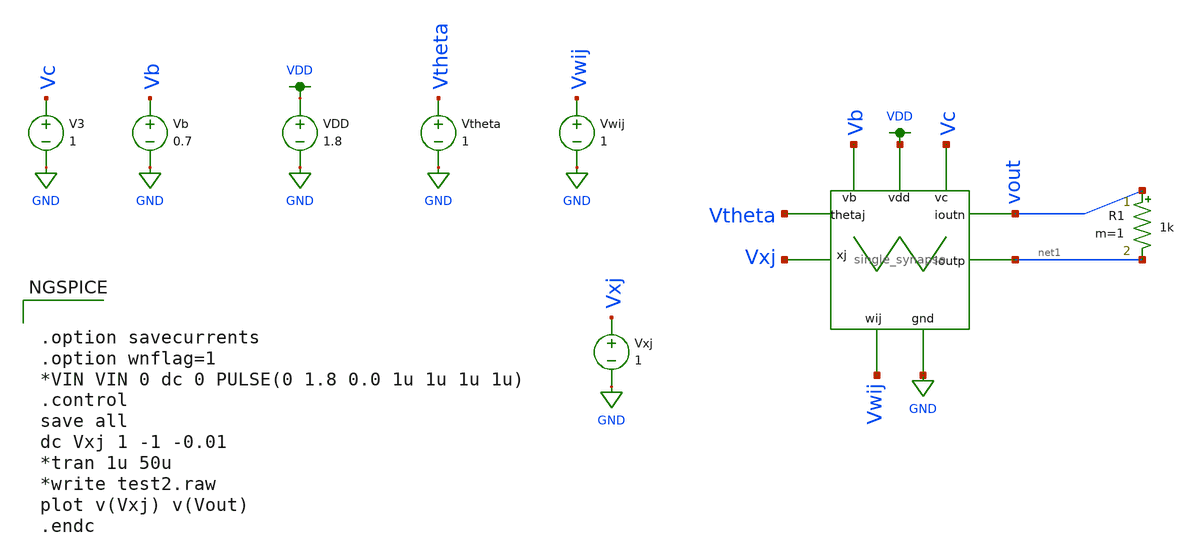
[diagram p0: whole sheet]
** sch_path: test_single_synapse.sch
**.subckt test_single_synapse
VDD VDD GND 1.8
Vb Vb GND 0.7
V3 Vc GND 1
W1 Vtheta Vb VDD Vc Vxj GND Vwij vout net1 single_synapse
Vtheta Vtheta GND 1
Vwij Vwij GND 1
Vxj Vxj GND 1
R1 vout net1 1k m=1
**** begin user architecture code


.option savecurrents
.option wnflag=1
*VIN VIN 0 dc 0 PULSE(0 1.8 0.0 1u 1u 1u 1u)
.control
save all
dc Vxj 1 -1 -0.01
*tran 1u 50u
*write test2.raw
plot v(Vxj) v(Vout)
.endc



.option wnflag=1
.lib ~/skywater/skywater-pdk/libraries/sky130_fd_pr_ngspice/latest/models/sky130.lib.spice tt

**** end user architecture code
**.ends

* expanding   symbol:  /home/ttuser/image_processing_final/single_synapse.sym # of pins=9
** sym_path: single_synapse.sym
** sch_path: single_synapse.sch
.subckt single_synapse thetaj Vb Vdd Vc xj GND Wij Ioutn Ioutp
*.iopin Ioutn
*.iopin Ioutp
*.iopin thetaj
*.iopin xj
*.iopin Wij
*.iopin Vb
*.iopin Vc
*.iopin GND
*.iopin Vdd
XM1 Ioutn Ioutn Vdd VDD sky130_fd_pr__pfet_01v8 L=0.15 W=1 nf=1 ad='int((nf+1)/2) * W/nf * 0.29' as='int((nf+2)/2) * W/nf * 0.29'
+ pd='2*int((nf+1)/2) * (W/nf + 0.29)' ps='2*int((nf+2)/2) * (W/nf + 0.29)' nrd='0.29 / W' nrs='0.29 / W'
+ sa=0 sb=0 sd=0 mult=1 m=1
XM2 Ioutp Ioutp Vdd VDD sky130_fd_pr__pfet_01v8 L=0.15 W=1 nf=1 ad='int((nf+1)/2) * W/nf * 0.29' as='int((nf+2)/2) * W/nf * 0.29'
+ pd='2*int((nf+1)/2) * (W/nf + 0.29)' ps='2*int((nf+2)/2) * (W/nf + 0.29)' nrd='0.29 / W' nrs='0.29 / W'
+ sa=0 sb=0 sd=0 mult=1 m=1
XM3 Ioutp xj net1 GND sky130_fd_pr__nfet_01v8 L=0.15 W=1 nf=1 ad='int((nf+1)/2) * W/nf * 0.29' as='int((nf+2)/2) * W/nf * 0.29'
+ pd='2*int((nf+1)/2) * (W/nf + 0.29)' ps='2*int((nf+2)/2) * (W/nf + 0.29)' nrd='0.29 / W' nrs='0.29 / W'
+ sa=0 sb=0 sd=0 mult=1 m=1
XM4 net1 net1 net3 GND sky130_fd_pr__nfet_01v8 L=0.15 W=1 nf=1 ad='int((nf+1)/2) * W/nf * 0.29' as='int((nf+2)/2) * W/nf * 0.29'
+ pd='2*int((nf+1)/2) * (W/nf + 0.29)' ps='2*int((nf+2)/2) * (W/nf + 0.29)' nrd='0.29 / W' nrs='0.29 / W'
+ sa=0 sb=0 sd=0 mult=1 m=1
XM5 Ioutn thetaj net2 GND sky130_fd_pr__nfet_01v8 L=0.15 W=1 nf=1 ad='int((nf+1)/2) * W/nf * 0.29' as='int((nf+2)/2) * W/nf * 0.29'
+ pd='2*int((nf+1)/2) * (W/nf + 0.29)' ps='2*int((nf+2)/2) * (W/nf + 0.29)' nrd='0.29 / W' nrs='0.29 / W'
+ sa=0 sb=0 sd=0 mult=1 m=1
XM6 net2 net2 net3 GND sky130_fd_pr__nfet_01v8 L=0.15 W=1 nf=1 ad='int((nf+1)/2) * W/nf * 0.29' as='int((nf+2)/2) * W/nf * 0.29'
+ pd='2*int((nf+1)/2) * (W/nf + 0.29)' ps='2*int((nf+2)/2) * (W/nf + 0.29)' nrd='0.29 / W' nrs='0.29 / W'
+ sa=0 sb=0 sd=0 mult=1 m=1
X1 Wij GND Wij Vc net3 Vdd triode
.ends


* expanding   symbol:  /home/ttuser/image_processing_final/triode.sym # of pins=9
** sym_path: triode.sym
** sch_path: triode.sch
.subckt triode Vin GND Vb Vc Vout Vdd
*.iopin Vout
*.iopin Vc
*.iopin Vb
*.iopin Vin
*.iopin GND
*.iopin Vdd
XM7 net4 net1 Vdd VDD sky130_fd_pr__pfet_01v8 L=0.15 W=1 nf=1 ad='int((nf+1)/2) * W/nf * 0.29' as='int((nf+2)/2) * W/nf * 0.29'
+ pd='2*int((nf+1)/2) * (W/nf + 0.29)' ps='2*int((nf+2)/2) * (W/nf + 0.29)' nrd='0.29 / W' nrs='0.29 / W'
+ sa=0 sb=0 sd=0 mult=1 m=1
XM6 net1 net1 Vdd VDD sky130_fd_pr__pfet_01v8 L=0.15 W=1 nf=1 ad='int((nf+1)/2) * W/nf * 0.29' as='int((nf+2)/2) * W/nf * 0.29'
+ pd='2*int((nf+1)/2) * (W/nf + 0.29)' ps='2*int((nf+2)/2) * (W/nf + 0.29)' nrd='0.29 / W' nrs='0.29 / W'
+ sa=0 sb=0 sd=0 mult=1 m=1
XM5 net1 Vc net2 GND sky130_fd_pr__nfet_01v8 L=0.15 W=1 nf=1 ad='int((nf+1)/2) * W/nf * 0.29' as='int((nf+2)/2) * W/nf * 0.29'
+ pd='2*int((nf+1)/2) * (W/nf + 0.29)' ps='2*int((nf+2)/2) * (W/nf + 0.29)' nrd='0.29 / W' nrs='0.29 / W'
+ sa=0 sb=0 sd=0 mult=1 m=1
XM1 GND net3 net2 VDD sky130_fd_pr__pfet_01v8 L=0.15 W=1 nf=1 ad='int((nf+1)/2) * W/nf * 0.29' as='int((nf+2)/2) * W/nf * 0.29'
+ pd='2*int((nf+1)/2) * (W/nf + 0.29)' ps='2*int((nf+2)/2) * (W/nf + 0.29)' nrd='0.29 / W' nrs='0.29 / W'
+ sa=0 sb=0 sd=0 mult=1 m=1
XM2 net4 Vb GND GND sky130_fd_pr__nfet_01v8 L=0.15 W=1 nf=1 ad='int((nf+1)/2) * W/nf * 0.29' as='int((nf+2)/2) * W/nf * 0.29'
+ pd='2*int((nf+1)/2) * (W/nf + 0.29)' ps='2*int((nf+2)/2) * (W/nf + 0.29)' nrd='0.29 / W' nrs='0.29 / W'
+ sa=0 sb=0 sd=0 mult=1 m=1
XM3 net3 Vin GND GND sky130_fd_pr__nfet_01v8 L=0.15 W=1 nf=1 ad='int((nf+1)/2) * W/nf * 0.29' as='int((nf+2)/2) * W/nf * 0.29'
+ pd='2*int((nf+1)/2) * (W/nf + 0.29)' ps='2*int((nf+2)/2) * (W/nf + 0.29)' nrd='0.29 / W' nrs='0.29 / W'
+ sa=0 sb=0 sd=0 mult=1 m=1
XM4 Vout net4 net3 GND sky130_fd_pr__nfet_01v8 L=0.15 W=1 nf=1 ad='int((nf+1)/2) * W/nf * 0.29' as='int((nf+2)/2) * W/nf * 0.29'
+ pd='2*int((nf+1)/2) * (W/nf + 0.29)' ps='2*int((nf+2)/2) * (W/nf + 0.29)' nrd='0.29 / W' nrs='0.29 / W'
+ sa=0 sb=0 sd=0 mult=1 m=1
.ends

.GLOBAL VDD
.GLOBAL GND
.end
